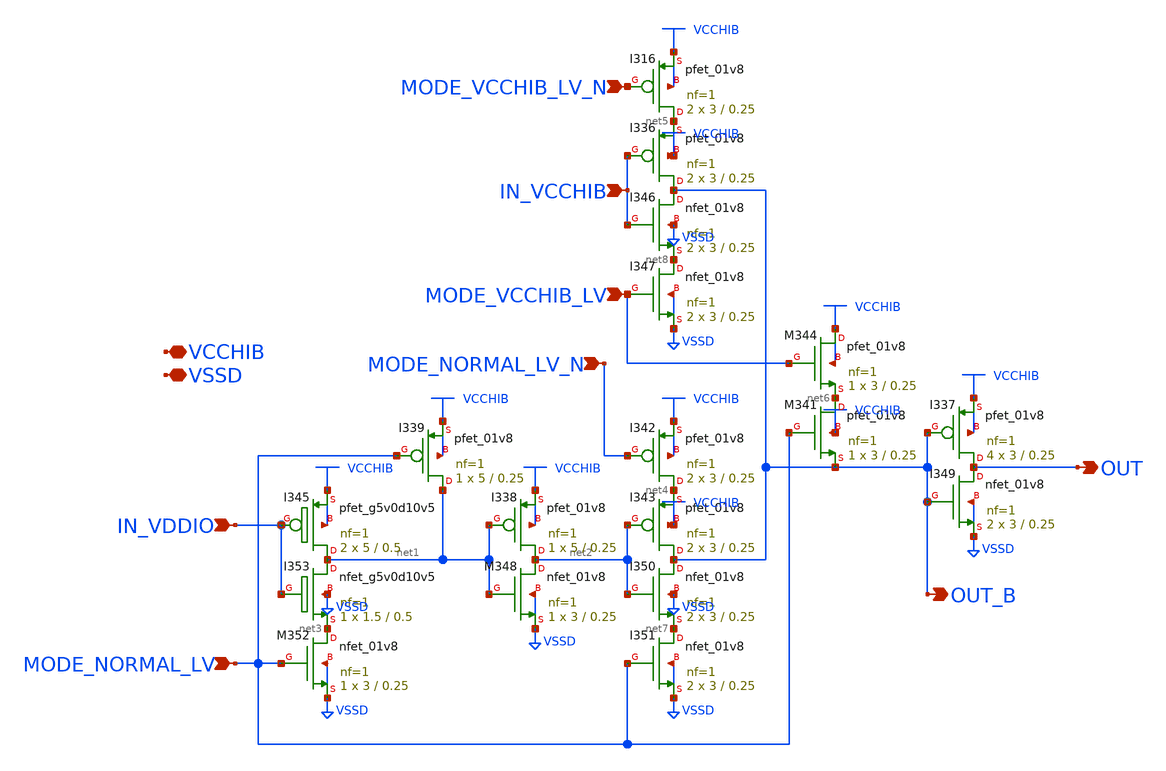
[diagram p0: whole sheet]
** sch_path: gpiov2_ipath_lvls.sch
* Copyright 2023 David Mitchell Bailey
* Licensed under the Apache License, Version 2.0 (the "License");
* you may not use this file except in compliance with the License.
* You may obtain a copy of the License at
* https://www.apache.org/licenses/LICENSE-2.0
* Unless required by applicable law or agreed to in writing, software
* distributed under the License is distributed on an "AS IS" BASIS,
* WITHOUT WARRANTIES OR CONDITIONS OF ANY KIND, either express or implied.
* See the License for the specific language governing permissions and
* limitations under the License.
**.subckt gpiov2_ipath_lvls IN_VDDIO VCCHIB VSSD OUT MODE_NORMAL_LV MODE_VCCHIB_LV_N MODE_VCCHIB_LV
*+ IN_VCCHIB MODE_NORMAL_LV_N OUT_B
*.ipin IN_VDDIO
*.iopin VCCHIB
*.iopin VSSD
*.opin OUT
*.ipin MODE_NORMAL_LV
*.ipin MODE_VCCHIB_LV_N
*.ipin MODE_VCCHIB_LV
*.ipin IN_VCCHIB
*.ipin MODE_NORMAL_LV_N
*.opin OUT_B
XI353 net1 IN_VDDIO net3 VSSD sky130_fd_pr__nfet_g5v0d10v5 L=0.5 W=1.5 nf=1 ad='int((nf+1)/2) * W/nf * 0.29'
+ as='int((nf+2)/2) * W/nf * 0.29' pd='2*int((nf+1)/2) * (W/nf + 0.29)' ps='2*int((nf+2)/2) * (W/nf + 0.29)'
+ nrd='0.29 / W' nrs='0.29 / W' sa=0 sb=0 sd=0 mult=1 m=1
XI345 net1 IN_VDDIO VCCHIB VCCHIB sky130_fd_pr__pfet_g5v0d10v5 L=0.5 W=5 nf=1 ad='int((nf+1)/2) * W/nf * 0.29'
+ as='int((nf+2)/2) * W/nf * 0.29' pd='2*int((nf+1)/2) * (W/nf + 0.29)' ps='2*int((nf+2)/2) * (W/nf + 0.29)'
+ nrd='0.29 / W' nrs='0.29 / W' sa=0 sb=0 sd=0 mult=2 m=2
XI339 net1 MODE_NORMAL_LV VCCHIB VCCHIB sky130_fd_pr__pfet_01v8 L=0.25 W=5 nf=1 ad='int((nf+1)/2) * W/nf * 0.29'
+ as='int((nf+2)/2) * W/nf * 0.29' pd='2*int((nf+1)/2) * (W/nf + 0.29)' ps='2*int((nf+2)/2) * (W/nf + 0.29)'
+ nrd='0.29 / W' nrs='0.29 / W' sa=0 sb=0 sd=0 mult=1 m=1
XI338 net2 net1 VCCHIB VCCHIB sky130_fd_pr__pfet_01v8 L=0.25 W=5 nf=1 ad='int((nf+1)/2) * W/nf * 0.29'
+ as='int((nf+2)/2) * W/nf * 0.29' pd='2*int((nf+1)/2) * (W/nf + 0.29)' ps='2*int((nf+2)/2) * (W/nf + 0.29)'
+ nrd='0.29 / W' nrs='0.29 / W' sa=0 sb=0 sd=0 mult=1 m=1
XI343 OUT_B net2 net4 VCCHIB sky130_fd_pr__pfet_01v8 L=0.25 W=3 nf=1 ad='int((nf+1)/2) * W/nf * 0.29'
+ as='int((nf+2)/2) * W/nf * 0.29' pd='2*int((nf+1)/2) * (W/nf + 0.29)' ps='2*int((nf+2)/2) * (W/nf + 0.29)'
+ nrd='0.29 / W' nrs='0.29 / W' sa=0 sb=0 sd=0 mult=2 m=2
XI342 net4 MODE_NORMAL_LV_N VCCHIB VCCHIB sky130_fd_pr__pfet_01v8 L=0.25 W=3 nf=1 ad='int((nf+1)/2) * W/nf * 0.29'
+ as='int((nf+2)/2) * W/nf * 0.29' pd='2*int((nf+1)/2) * (W/nf + 0.29)' ps='2*int((nf+2)/2) * (W/nf + 0.29)'
+ nrd='0.29 / W' nrs='0.29 / W' sa=0 sb=0 sd=0 mult=2 m=2
XI336 OUT_B IN_VCCHIB net5 VCCHIB sky130_fd_pr__pfet_01v8 L=0.25 W=3 nf=1 ad='int((nf+1)/2) * W/nf * 0.29'
+ as='int((nf+2)/2) * W/nf * 0.29' pd='2*int((nf+1)/2) * (W/nf + 0.29)' ps='2*int((nf+2)/2) * (W/nf + 0.29)'
+ nrd='0.29 / W' nrs='0.29 / W' sa=0 sb=0 sd=0 mult=2 m=2
XI316 net5 MODE_VCCHIB_LV_N VCCHIB VCCHIB sky130_fd_pr__pfet_01v8 L=0.25 W=3 nf=1 ad='int((nf+1)/2) * W/nf * 0.29'
+ as='int((nf+2)/2) * W/nf * 0.29' pd='2*int((nf+1)/2) * (W/nf + 0.29)' ps='2*int((nf+2)/2) * (W/nf + 0.29)'
+ nrd='0.29 / W' nrs='0.29 / W' sa=0 sb=0 sd=0 mult=2 m=2
XI337 OUT OUT_B VCCHIB VCCHIB sky130_fd_pr__pfet_01v8 L=0.25 W=3 nf=1 ad='int((nf+1)/2) * W/nf * 0.29'
+ as='int((nf+2)/2) * W/nf * 0.29' pd='2*int((nf+1)/2) * (W/nf + 0.29)' ps='2*int((nf+2)/2) * (W/nf + 0.29)'
+ nrd='0.29 / W' nrs='0.29 / W' sa=0 sb=0 sd=0 mult=4 m=4
XM341 net6 MODE_NORMAL_LV OUT_B VCCHIB sky130_fd_pr__pfet_01v8 L=0.25 W=3 nf=1 ad='int((nf+1)/2) * W/nf * 0.29'
+ as='int((nf+2)/2) * W/nf * 0.29' pd='2*int((nf+1)/2) * (W/nf + 0.29)' ps='2*int((nf+2)/2) * (W/nf + 0.29)'
+ nrd='0.29 / W' nrs='0.29 / W' sa=0 sb=0 sd=0 mult=1 m=1
XM344 VCCHIB MODE_VCCHIB_LV net6 VCCHIB sky130_fd_pr__pfet_01v8 L=0.25 W=3 nf=1 ad='int((nf+1)/2) * W/nf * 0.29'
+ as='int((nf+2)/2) * W/nf * 0.29' pd='2*int((nf+1)/2) * (W/nf + 0.29)' ps='2*int((nf+2)/2) * (W/nf + 0.29)'
+ nrd='0.29 / W' nrs='0.29 / W' sa=0 sb=0 sd=0 mult=1 m=1
XM352 net3 MODE_NORMAL_LV VSSD VSSD sky130_fd_pr__nfet_01v8 L=0.25 W=3 nf=1 ad='int((nf+1)/2) * W/nf * 0.29'
+ as='int((nf+2)/2) * W/nf * 0.29' pd='2*int((nf+1)/2) * (W/nf + 0.29)' ps='2*int((nf+2)/2) * (W/nf + 0.29)'
+ nrd='0.29 / W' nrs='0.29 / W' sa=0 sb=0 sd=0 mult=1 m=1
XM348 net2 net1 VSSD VSSD sky130_fd_pr__nfet_01v8 L=0.25 W=3 nf=1 ad='int((nf+1)/2) * W/nf * 0.29' as='int((nf+2)/2) * W/nf * 0.29'
+ pd='2*int((nf+1)/2) * (W/nf + 0.29)' ps='2*int((nf+2)/2) * (W/nf + 0.29)' nrd='0.29 / W' nrs='0.29 / W'
+ sa=0 sb=0 sd=0 mult=1 m=1
XI350 OUT_B net2 net7 VSSD sky130_fd_pr__nfet_01v8 L=0.25 W=3 nf=1 ad='int((nf+1)/2) * W/nf * 0.29' as='int((nf+2)/2) * W/nf * 0.29'
+ pd='2*int((nf+1)/2) * (W/nf + 0.29)' ps='2*int((nf+2)/2) * (W/nf + 0.29)' nrd='0.29 / W' nrs='0.29 / W'
+ sa=0 sb=0 sd=0 mult=2 m=2
XI351 net7 MODE_NORMAL_LV VSSD VSSD sky130_fd_pr__nfet_01v8 L=0.25 W=3 nf=1 ad='int((nf+1)/2) * W/nf * 0.29'
+ as='int((nf+2)/2) * W/nf * 0.29' pd='2*int((nf+1)/2) * (W/nf + 0.29)' ps='2*int((nf+2)/2) * (W/nf + 0.29)'
+ nrd='0.29 / W' nrs='0.29 / W' sa=0 sb=0 sd=0 mult=2 m=2
XI349 OUT OUT_B VSSD VSSD sky130_fd_pr__nfet_01v8 L=0.25 W=3 nf=1 ad='int((nf+1)/2) * W/nf * 0.29' as='int((nf+2)/2) * W/nf * 0.29'
+ pd='2*int((nf+1)/2) * (W/nf + 0.29)' ps='2*int((nf+2)/2) * (W/nf + 0.29)' nrd='0.29 / W' nrs='0.29 / W'
+ sa=0 sb=0 sd=0 mult=2 m=2
XI346 OUT_B IN_VCCHIB net8 VSSD sky130_fd_pr__nfet_01v8 L=0.25 W=3 nf=1 ad='int((nf+1)/2) * W/nf * 0.29'
+ as='int((nf+2)/2) * W/nf * 0.29' pd='2*int((nf+1)/2) * (W/nf + 0.29)' ps='2*int((nf+2)/2) * (W/nf + 0.29)'
+ nrd='0.29 / W' nrs='0.29 / W' sa=0 sb=0 sd=0 mult=2 m=2
XI347 net8 MODE_VCCHIB_LV VSSD VSSD sky130_fd_pr__nfet_01v8 L=0.25 W=3 nf=1 ad='int((nf+1)/2) * W/nf * 0.29'
+ as='int((nf+2)/2) * W/nf * 0.29' pd='2*int((nf+1)/2) * (W/nf + 0.29)' ps='2*int((nf+2)/2) * (W/nf + 0.29)'
+ nrd='0.29 / W' nrs='0.29 / W' sa=0 sb=0 sd=0 mult=2 m=2
**.ends
.end
